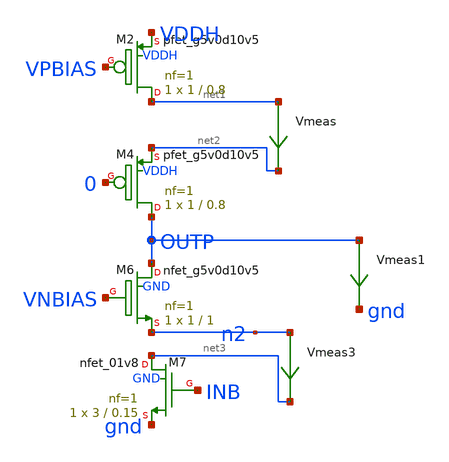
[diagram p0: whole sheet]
** sch_path: xschem/lvsf2-tb.sch
.lib $::SKYWATER_MODELS/sky130.lib.spice tt
.include $::SKYWATER_STDCELLS/sky130_fd_sc_hd.spice

**.subckt lvsf2-tb
Vmeas net1 net2 0
.save i(vmeas)
XM2 net1 VPBIAS VDDH VDDH sky130_fd_pr__pfet_g5v0d10v5 L=0.8 W=1 nf=1 ad='int((nf+1)/2) * W/nf * 0.29'
+ as='int((nf+2)/2) * W/nf * 0.29' pd='2*int((nf+1)/2) * (W/nf + 0.29)' ps='2*int((nf+2)/2) * (W/nf + 0.29)'
+ nrd='0.29 / W' nrs='0.29 / W' sa=0 sb=0 sd=0 mult=1 m=1
XM4 OUTP 0 net2 VDDH sky130_fd_pr__pfet_g5v0d10v5 L=0.8 W=1 nf=1 ad='int((nf+1)/2) * W/nf * 0.29' as='int((nf+2)/2) * W/nf * 0.29'
+ pd='2*int((nf+1)/2) * (W/nf + 0.29)' ps='2*int((nf+2)/2) * (W/nf + 0.29)' nrd='0.29 / W' nrs='0.29 / W'
+ sa=0 sb=0 sd=0 mult=1 m=1
XM6 OUTP VNBIAS n2 GND sky130_fd_pr__nfet_g5v0d10v5 L=1 W=1 nf=1 ad='int((nf+1)/2) * W/nf * 0.29' as='int((nf+2)/2) * W/nf * 0.29'
+ pd='2*int((nf+1)/2) * (W/nf + 0.29)' ps='2*int((nf+2)/2) * (W/nf + 0.29)' nrd='0.29 / W' nrs='0.29 / W'
+ sa=0 sb=0 sd=0 mult=1 m=1
XM7 net3 INB gnd GND sky130_fd_pr__nfet_01v8 L=0.15 W=3 nf=1 ad='int((nf+1)/2) * W/nf * 0.29' as='int((nf+2)/2) * W/nf * 0.29'
+ pd='2*int((nf+1)/2) * (W/nf + 0.29)' ps='2*int((nf+2)/2) * (W/nf + 0.29)' nrd='0.29 / W' nrs='0.29 / W'
+ sa=0 sb=0 sd=0 mult=1 m=1
Vmeas3 n2 net3 0
.save i(vmeas3)
Vmeas1 OUTP gnd 0
.save i(vmeas1)
**** begin user architecture code



  .param max_freq=100e3 period={1/max_freq} time_high={period/2}
  .param delay_vin1={time_high} delay_vin2={time_high*1.5}
  .param lval=100u

  .option wnflag=1
  .option safecurrents

  Vddh vddh gnd dc 5.5
  *Vin  in  gnd pulse(0 1.8 {delay_vin1} 1p 1p {time_high} {period})
  *Vinb inb gnd pulse(1.8 0 {delay_vin1} 1p 1p {time_high} {period})
  *vin in gnd 1.8
  vinb inb gnd 0
  vpb vpbias gnd 1.3273
  vnb vnbias gnd 1.1965
  .control
     reset
     save all
     *tran 0.1n 25u
     dc vpb 0 5.5 0.01
     write lvsf2-tb.raw
     set appendwrite
*    quit 0
  .endc



**** end user architecture code
**.ends
.end
